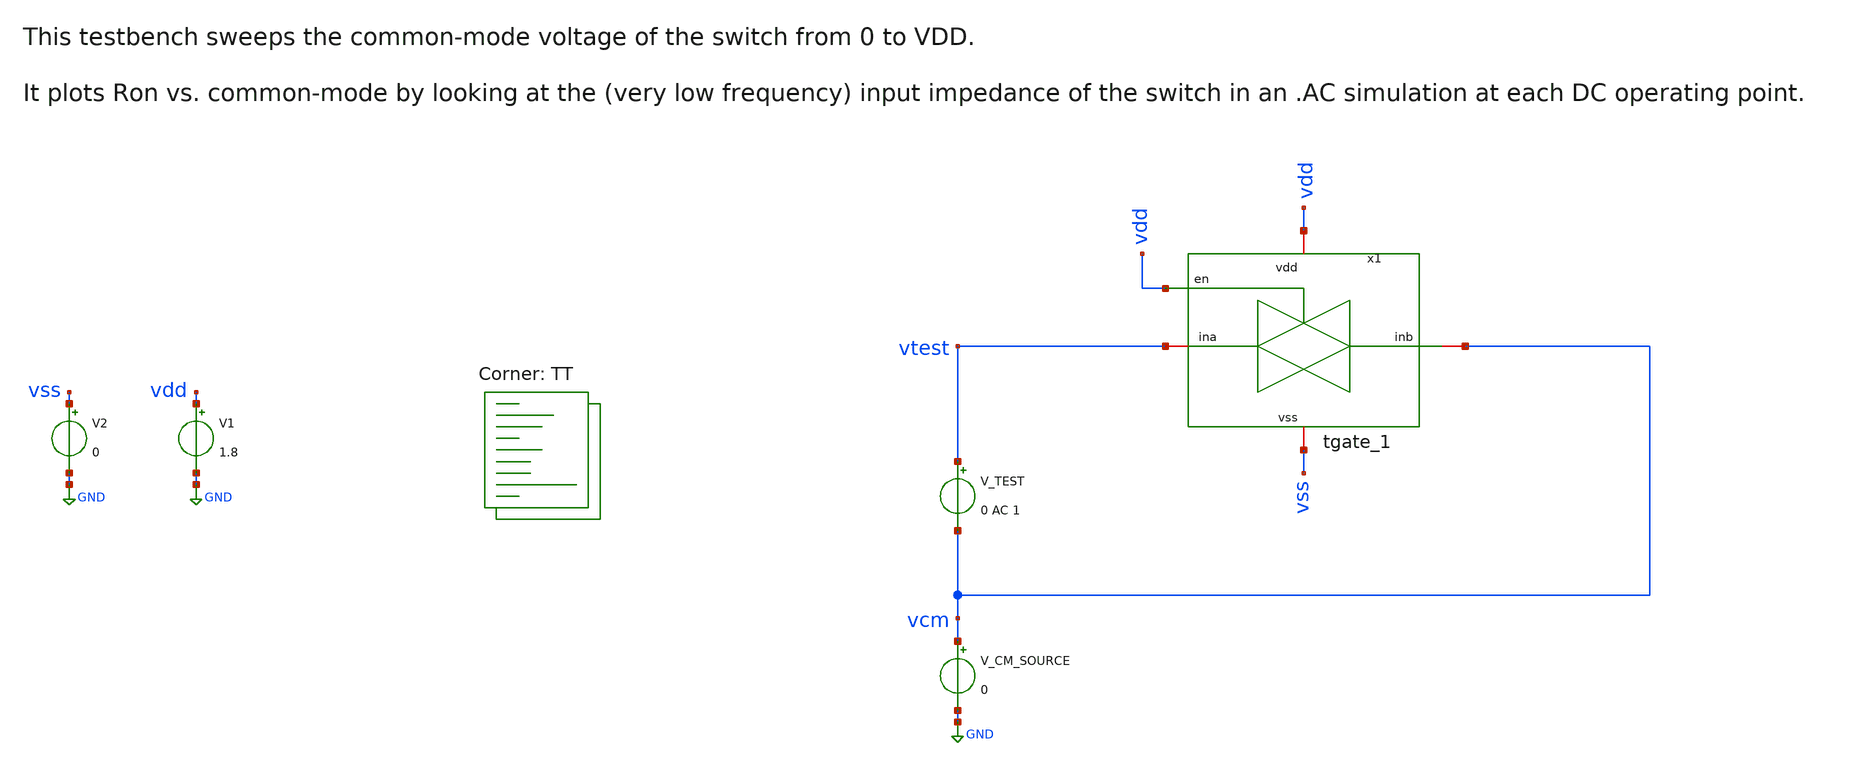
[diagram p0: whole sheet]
** sch_path: xsch/tb/tgate_1/tb_tgate1_ron_vs_vcm.sch
**.subckt tb_tgate1_ron_vs_vcm
V1 vdd GND 1.8
V2 vss GND 0
V_CM_SOURCE vcm GND 0
V_TEST vtest vcm 0 AC 1
.save i(v_test)
x1 vdd vdd vcm vtest vss tgate_1
**** begin user architecture code


.option method = gear
*.param TEMPGAUSS = agauss(40, 30, 1)
*.option temp = 'TEMPGAUSS'

.control

	let loops = 1000
	let vecvcm = vector(loops)
	let Ron = vector(loops);
	let vcmm = 0
	let index = 0

	repeat $&loops
		alter V_CM_SOURCE $&vcmm;
		ac dec 1 0.1 1
		let index = index+1;

		meas ac itest find i(v_test) at=0.1

		let Ron[index] = 1/mag(itest);
		let vecvcm[index] = vcmm;
		let vcmm = vcmm + 0.0018;
	end

set nolegend
plot Ron vs vecvcm xlabel 'Common-Mode Voltage [V]' ylabel 'Switch Resistance [Ohms]' xlimit 0 1.6

rusage
.endc

.end


.lib $::SKYWATER_MODELS/sky130.lib.spice TT
**** end user architecture code
**.ends
.GLOBAL GND
.end
